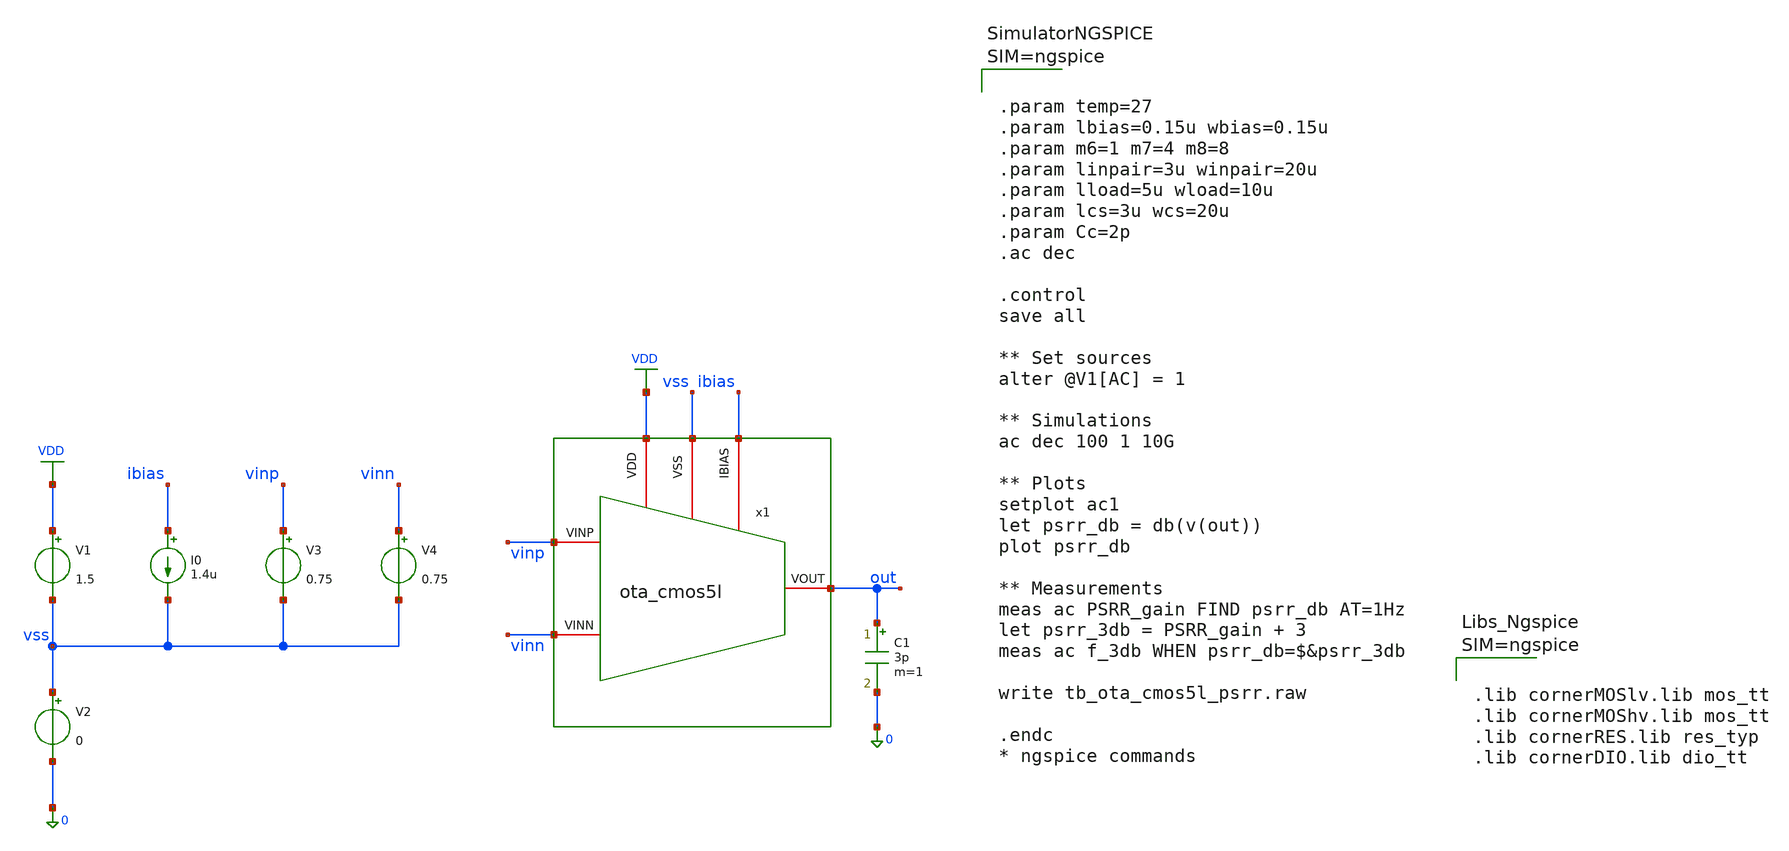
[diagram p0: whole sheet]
** sch_path: xschem/ota_cmos5l/tb/tb_ota_cmos5l_psrr/tb_ota_cmos5l_psrr.sch
**.subckt tb_ota_cmos5l_psrr
x1 vss ibias VDD vinn vinp out ota_cmos5l
C1 out 0 3p m=1
I0 ibias vss 1.4u
V1 VDD vss 1.5
V2 vss 0 0
V3 vinp vss 0.75
V4 vinn vss 0.75
**** begin user architecture code



.param temp=27
.param lbias=0.15u wbias=0.15u
.param m6=1 m7=4 m8=8
.param linpair=3u winpair=20u
.param lload=5u wload=10u
.param lcs=3u wcs=20u
.param Cc=2p
.ac dec

.control
save all

** Set sources
alter @V1[AC] = 1

** Simulations
ac dec 100 1 10G

** Plots
setplot ac1
let psrr_db = db(v(out))
plot psrr_db

** Measurements
meas ac PSRR_gain FIND psrr_db AT=1Hz
let psrr_3db = PSRR_gain + 3
meas ac f_3db WHEN psrr_db=$&psrr_3db

write tb_ota_cmos5l_psrr.raw

.endc
* ngspice commands






.lib cornerMOSlv.lib mos_tt
.lib cornerMOShv.lib mos_tt
.lib cornerRES.lib res_typ
.lib cornerDIO.lib dio_tt



**** end user architecture code
**.ends

* expanding   symbol:  /foss/designs/sg13cmos5l_spma_ip__instramp/xschem/ota_cmos5l/ota_cmos5l.sym #
*+ of pins=6
** sym_path: xschem/output_buffer/ota_cmos5l.sym
** sch_path: xschem/output_buffer/ota_cmos5l.sch
.subckt ota_cmos5l VSS IBIAS VDD VINN VINP VOUT
*.iopin IBIAS
*.iopin VDD
*.iopin VSS
*.iopin VOUT
*.iopin VINP
*.iopin VINN
XM6 IBIAS IBIAS VDD VDD sg13_lv_pmos w={wbias} l={lbias} ng=1 m={m6} mm_ok=1
XM7 net1 IBIAS VDD VDD sg13_lv_pmos w={wbias} l={lbias} ng=1 m={m7} mm_ok=1
XM8 VOUT IBIAS VDD VDD sg13_lv_pmos w={wbias} l={lbias} ng=1 m={m8} mm_ok=1
XM1 net2 VINN net1 VDD sg13_lv_pmos w={winpair} l={linpair} ng=1 m=1 mm_ok=1
XM2 net3 VINP net1 VDD sg13_lv_pmos w={winpair} l={linpair} ng=1 m=1 mm_ok=1
XM3 net2 net2 VSS VSS sg13_lv_nmos w={wload} l={lload} ng=1 m=1 mm_ok=1
XM4 net3 net2 VSS VSS sg13_lv_nmos w={wload} l={lload} ng=1 m=1 mm_ok=1
XM5 VOUT net3 VSS VSS sg13_lv_nmos w={wcs} l={lcs} ng=1 m=1 mm_ok=1
XR1 net3 net4 VSS rhigh w=0.5e-6 l=1.95e-6 m=1 b=0 mm_ok=1
.save v(vinp)
.save v(vinn)
.save v(vout)
XC2 VOUT net4 cap_cmomi w=15e-6 l=15e-6 mmin=1 mmax=4 feed=double subblock=0 m=5 mm_ok=1
**** begin user architecture code


.param temp=27
.param lbias=0.15u wbias=0.15u
.param m6=1 m7=4 m8=8
.param linpair=3u winpair=20u
.param lload=5u wload=10u
.param lcs=3u wcs=20u
.param Cc=2p



**** end user architecture code
XC1 VOUT net4 cap_cmomi w=15e-6 l=15e-6 mmin=1 mmax=4 feed=double subblock=0 m=4 mm_ok=1
.ends

.GLOBAL VDD
.end
